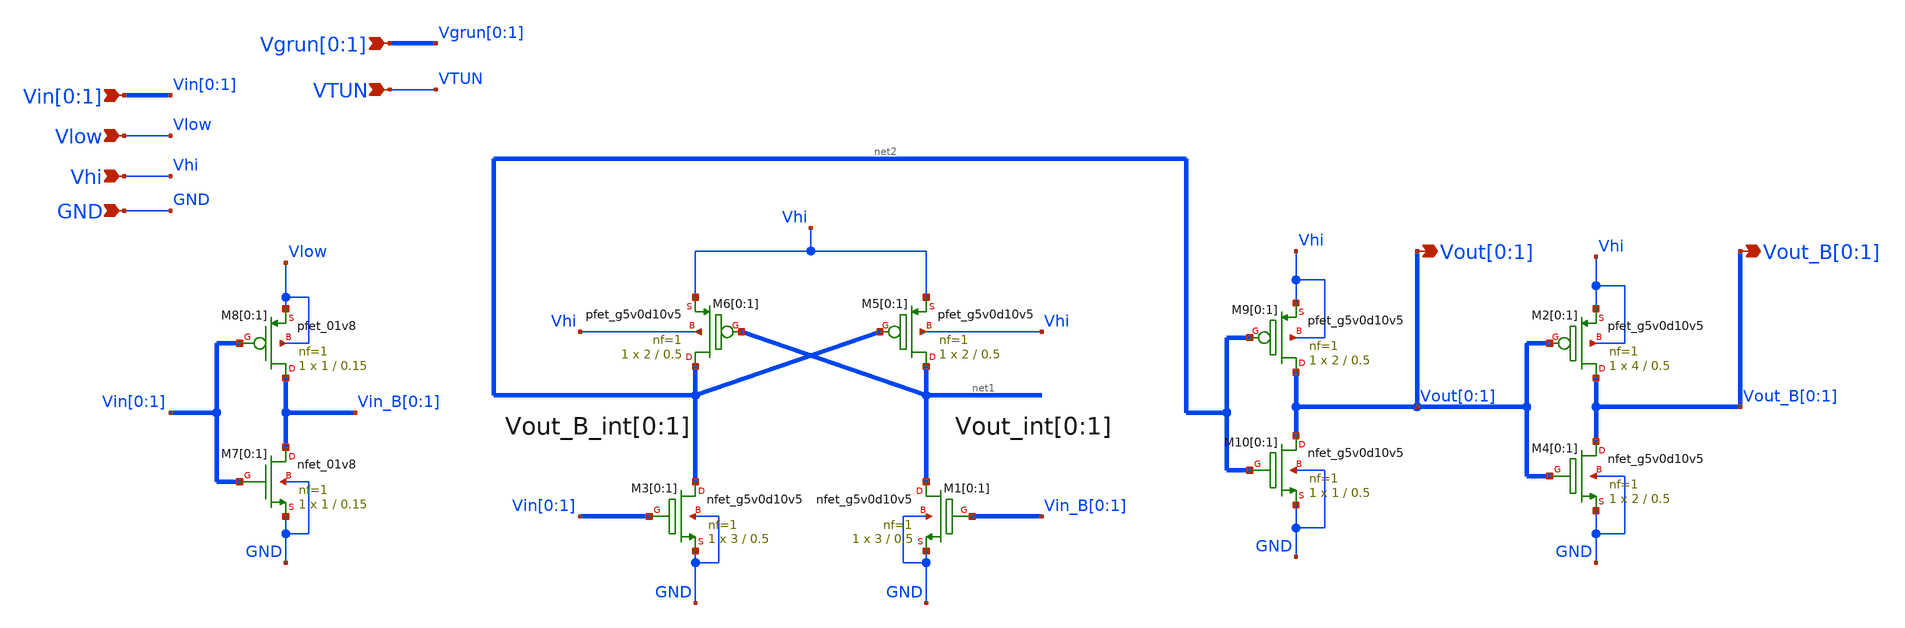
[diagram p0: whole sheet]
** sch_path: sky130_cells/Level_Shifter/Vertical_LS/level_shifter_vertical.sch
* Copyright 2021 Stefan Frederik Schippers
* Licensed under the Apache License, Version 2.0 (the "License");
* you may not use this file except in compliance with the License.
* You may obtain a copy of the License at
* https://www.apache.org/licenses/LICENSE-2.0
* Unless required by applicable law or agreed to in writing, software
* distributed under the License is distributed on an "AS IS" BASIS,
* WITHOUT WARRANTIES OR CONDITIONS OF ANY KIND, either express or implied.
* See the License for the specific language governing permissions and
* limitations under the License.
**.subckt level_shifter_vertical Vlow Vhi Vin[0],Vin[1] Vout[0],Vout[1] GND Vout_B[0],Vout_B[1] VTUN
*+ Vgrun[0],Vgrun[1]
*.ipin Vlow
*.ipin Vhi
*.ipin Vin[0],Vin[1]
*.opin Vout[0],Vout[1]
*.ipin GND
*.opin Vout_B[0],Vout_B[1]
*.ipin VTUN
*.ipin Vgrun[0],Vgrun[1]
XM5[0] net1[1] net2[1] Vhi Vhi sky130_fd_pr__pfet_g5v0d10v5 L=0.5 W=2 nf=1 ad='int((nf+1)/2) * W/nf * 0.29'
+ as='int((nf+2)/2) * W/nf * 0.29' pd='2*int((nf+1)/2) * (W/nf + 0.29)' ps='2*int((nf+2)/2) * (W/nf + 0.29)'
+ nrd='0.29 / W' nrs='0.29 / W' sa=0 sb=0 sd=0 mult=1 m=1
XM5[1] net1[0] net2[0] Vhi Vhi sky130_fd_pr__pfet_g5v0d10v5 L=0.5 W=2 nf=1 ad='int((nf+1)/2) * W/nf * 0.29'
+ as='int((nf+2)/2) * W/nf * 0.29' pd='2*int((nf+1)/2) * (W/nf + 0.29)' ps='2*int((nf+2)/2) * (W/nf + 0.29)'
+ nrd='0.29 / W' nrs='0.29 / W' sa=0 sb=0 sd=0 mult=1 m=1
XM6[0] net2[1] net1[1] Vhi Vhi sky130_fd_pr__pfet_g5v0d10v5 L=0.5 W=2 nf=1 ad='int((nf+1)/2) * W/nf * 0.29'
+ as='int((nf+2)/2) * W/nf * 0.29' pd='2*int((nf+1)/2) * (W/nf + 0.29)' ps='2*int((nf+2)/2) * (W/nf + 0.29)'
+ nrd='0.29 / W' nrs='0.29 / W' sa=0 sb=0 sd=0 mult=1 m=1
XM6[1] net2[0] net1[0] Vhi Vhi sky130_fd_pr__pfet_g5v0d10v5 L=0.5 W=2 nf=1 ad='int((nf+1)/2) * W/nf * 0.29'
+ as='int((nf+2)/2) * W/nf * 0.29' pd='2*int((nf+1)/2) * (W/nf + 0.29)' ps='2*int((nf+2)/2) * (W/nf + 0.29)'
+ nrd='0.29 / W' nrs='0.29 / W' sa=0 sb=0 sd=0 mult=1 m=1
XM7[0] Vin_B[0] Vin[0] GND GND sky130_fd_pr__nfet_01v8 L=0.15 W=1 nf=1 ad='int((nf+1)/2) * W/nf * 0.29'
+ as='int((nf+2)/2) * W/nf * 0.29' pd='2*int((nf+1)/2) * (W/nf + 0.29)' ps='2*int((nf+2)/2) * (W/nf + 0.29)'
+ nrd='0.29 / W' nrs='0.29 / W' sa=0 sb=0 sd=0 mult=1 m=1
XM7[1] Vin_B[1] Vin[1] GND GND sky130_fd_pr__nfet_01v8 L=0.15 W=1 nf=1 ad='int((nf+1)/2) * W/nf * 0.29'
+ as='int((nf+2)/2) * W/nf * 0.29' pd='2*int((nf+1)/2) * (W/nf + 0.29)' ps='2*int((nf+2)/2) * (W/nf + 0.29)'
+ nrd='0.29 / W' nrs='0.29 / W' sa=0 sb=0 sd=0 mult=1 m=1
XM8[0] Vin_B[0] Vin[0] Vlow Vlow sky130_fd_pr__pfet_01v8 L=0.15 W=1 nf=1 ad='int((nf+1)/2) * W/nf * 0.29'
+ as='int((nf+2)/2) * W/nf * 0.29' pd='2*int((nf+1)/2) * (W/nf + 0.29)' ps='2*int((nf+2)/2) * (W/nf + 0.29)'
+ nrd='0.29 / W' nrs='0.29 / W' sa=0 sb=0 sd=0 mult=1 m=1
XM8[1] Vin_B[1] Vin[1] Vlow Vlow sky130_fd_pr__pfet_01v8 L=0.15 W=1 nf=1 ad='int((nf+1)/2) * W/nf * 0.29'
+ as='int((nf+2)/2) * W/nf * 0.29' pd='2*int((nf+1)/2) * (W/nf + 0.29)' ps='2*int((nf+2)/2) * (W/nf + 0.29)'
+ nrd='0.29 / W' nrs='0.29 / W' sa=0 sb=0 sd=0 mult=1 m=1
XM9[0] Vout[0] net2[1] Vhi Vhi sky130_fd_pr__pfet_g5v0d10v5 L=0.5 W=2 nf=1 ad='int((nf+1)/2) * W/nf * 0.29'
+ as='int((nf+2)/2) * W/nf * 0.29' pd='2*int((nf+1)/2) * (W/nf + 0.29)' ps='2*int((nf+2)/2) * (W/nf + 0.29)'
+ nrd='0.29 / W' nrs='0.29 / W' sa=0 sb=0 sd=0 mult=1 m=1
XM9[1] Vout[1] net2[0] Vhi Vhi sky130_fd_pr__pfet_g5v0d10v5 L=0.5 W=2 nf=1 ad='int((nf+1)/2) * W/nf * 0.29'
+ as='int((nf+2)/2) * W/nf * 0.29' pd='2*int((nf+1)/2) * (W/nf + 0.29)' ps='2*int((nf+2)/2) * (W/nf + 0.29)'
+ nrd='0.29 / W' nrs='0.29 / W' sa=0 sb=0 sd=0 mult=1 m=1
XM10[0] Vout[0] net2[1] GND GND sky130_fd_pr__nfet_g5v0d10v5 L=0.5 W=1 nf=1 ad='int((nf+1)/2) * W/nf * 0.29'
+ as='int((nf+2)/2) * W/nf * 0.29' pd='2*int((nf+1)/2) * (W/nf + 0.29)' ps='2*int((nf+2)/2) * (W/nf + 0.29)'
+ nrd='0.29 / W' nrs='0.29 / W' sa=0 sb=0 sd=0 mult=1 m=1
XM10[1] Vout[1] net2[0] GND GND sky130_fd_pr__nfet_g5v0d10v5 L=0.5 W=1 nf=1 ad='int((nf+1)/2) * W/nf * 0.29'
+ as='int((nf+2)/2) * W/nf * 0.29' pd='2*int((nf+1)/2) * (W/nf + 0.29)' ps='2*int((nf+2)/2) * (W/nf + 0.29)'
+ nrd='0.29 / W' nrs='0.29 / W' sa=0 sb=0 sd=0 mult=1 m=1
XM3[0] net2[1] Vin[0] GND GND sky130_fd_pr__nfet_g5v0d10v5 L=0.5 W=3 nf=1 ad='int((nf+1)/2) * W/nf * 0.29'
+ as='int((nf+2)/2) * W/nf * 0.29' pd='2*int((nf+1)/2) * (W/nf + 0.29)' ps='2*int((nf+2)/2) * (W/nf + 0.29)'
+ nrd='0.29 / W' nrs='0.29 / W' sa=0 sb=0 sd=0 mult=1 m=1
XM3[1] net2[0] Vin[1] GND GND sky130_fd_pr__nfet_g5v0d10v5 L=0.5 W=3 nf=1 ad='int((nf+1)/2) * W/nf * 0.29'
+ as='int((nf+2)/2) * W/nf * 0.29' pd='2*int((nf+1)/2) * (W/nf + 0.29)' ps='2*int((nf+2)/2) * (W/nf + 0.29)'
+ nrd='0.29 / W' nrs='0.29 / W' sa=0 sb=0 sd=0 mult=1 m=1
XM1[0] net1[1] Vin_B[0] GND GND sky130_fd_pr__nfet_g5v0d10v5 L=0.5 W=3 nf=1 ad='int((nf+1)/2) * W/nf * 0.29'
+ as='int((nf+2)/2) * W/nf * 0.29' pd='2*int((nf+1)/2) * (W/nf + 0.29)' ps='2*int((nf+2)/2) * (W/nf + 0.29)'
+ nrd='0.29 / W' nrs='0.29 / W' sa=0 sb=0 sd=0 mult=1 m=1
XM1[1] net1[0] Vin_B[1] GND GND sky130_fd_pr__nfet_g5v0d10v5 L=0.5 W=3 nf=1 ad='int((nf+1)/2) * W/nf * 0.29'
+ as='int((nf+2)/2) * W/nf * 0.29' pd='2*int((nf+1)/2) * (W/nf + 0.29)' ps='2*int((nf+2)/2) * (W/nf + 0.29)'
+ nrd='0.29 / W' nrs='0.29 / W' sa=0 sb=0 sd=0 mult=1 m=1
XM2[0] Vout_B[0] Vout[0] Vhi Vhi sky130_fd_pr__pfet_g5v0d10v5 L=0.5 W=4 nf=1 ad='int((nf+1)/2) * W/nf * 0.29'
+ as='int((nf+2)/2) * W/nf * 0.29' pd='2*int((nf+1)/2) * (W/nf + 0.29)' ps='2*int((nf+2)/2) * (W/nf + 0.29)'
+ nrd='0.29 / W' nrs='0.29 / W' sa=0 sb=0 sd=0 mult=1 m=1
XM2[1] Vout_B[1] Vout[1] Vhi Vhi sky130_fd_pr__pfet_g5v0d10v5 L=0.5 W=4 nf=1 ad='int((nf+1)/2) * W/nf * 0.29'
+ as='int((nf+2)/2) * W/nf * 0.29' pd='2*int((nf+1)/2) * (W/nf + 0.29)' ps='2*int((nf+2)/2) * (W/nf + 0.29)'
+ nrd='0.29 / W' nrs='0.29 / W' sa=0 sb=0 sd=0 mult=1 m=1
XM4[0] Vout_B[0] Vout[0] GND GND sky130_fd_pr__nfet_g5v0d10v5 L=0.5 W=2 nf=1 ad='int((nf+1)/2) * W/nf * 0.29'
+ as='int((nf+2)/2) * W/nf * 0.29' pd='2*int((nf+1)/2) * (W/nf + 0.29)' ps='2*int((nf+2)/2) * (W/nf + 0.29)'
+ nrd='0.29 / W' nrs='0.29 / W' sa=0 sb=0 sd=0 mult=1 m=1
XM4[1] Vout_B[1] Vout[1] GND GND sky130_fd_pr__nfet_g5v0d10v5 L=0.5 W=2 nf=1 ad='int((nf+1)/2) * W/nf * 0.29'
+ as='int((nf+2)/2) * W/nf * 0.29' pd='2*int((nf+1)/2) * (W/nf + 0.29)' ps='2*int((nf+2)/2) * (W/nf + 0.29)'
+ nrd='0.29 / W' nrs='0.29 / W' sa=0 sb=0 sd=0 mult=1 m=1
**.ends
.end
